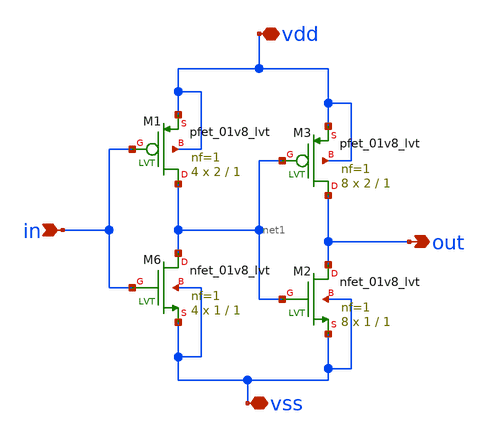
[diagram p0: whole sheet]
** sch_path: buffer.sch
**.subckt buffer in out vdd vss
*.ipin in
*.opin out
*.iopin vdd
*.iopin vss
XM6 net1 in vss vss sky130_fd_pr__nfet_01v8_lvt L=1 W=1 nf=1 ad='int((1 + 1)/2) * 1 / 1 * 0.29' as='int((1 + 2)/2) * 1 / 1 * 0.29'
+ pd='2*int((1 + 1)/2) * (1 / 1 + 0.29)' ps='2*int((1 + 2)/2) * (1 / 1 + 0.29)' nrd='0.29 / 1 ' nrs='0.29 / 1 '
+ sa=0 sb=0 sd=0 mult=4 m=4
XM1 net1 in vdd vdd sky130_fd_pr__pfet_01v8_lvt L=1 W=2 nf=1 ad='int((1 + 1)/2) * 2 / 1 * 0.29' as='int((1 + 2)/2) * 2 / 1 * 0.29'
+ pd='2*int((1 + 1)/2) * (2 / 1 + 0.29)' ps='2*int((1 + 2)/2) * (2 / 1 + 0.29)' nrd='0.29 / 2 ' nrs='0.29 / 2 '
+ sa=0 sb=0 sd=0 mult=4 m=4
XM2 out net1 vss vss sky130_fd_pr__nfet_01v8_lvt L=1 W=1 nf=1 ad='int((1 + 1)/2) * 1 / 1 * 0.29' as='int((1 + 2)/2) * 1 / 1 * 0.29'
+ pd='2*int((1 + 1)/2) * (1 / 1 + 0.29)' ps='2*int((1 + 2)/2) * (1 / 1 + 0.29)' nrd='0.29 / 1 ' nrs='0.29 / 1 '
+ sa=0 sb=0 sd=0 mult=8 m=8
XM3 out net1 vdd vdd sky130_fd_pr__pfet_01v8_lvt L=1 W=2 nf=1 ad='int((1 + 1)/2) * 2 / 1 * 0.29' as='int((1 + 2)/2) * 2 / 1 * 0.29'
+ pd='2*int((1 + 1)/2) * (2 / 1 + 0.29)' ps='2*int((1 + 2)/2) * (2 / 1 + 0.29)' nrd='0.29 / 2 ' nrs='0.29 / 2 '
+ sa=0 sb=0 sd=0 mult=8 m=8
**.ends
.end
